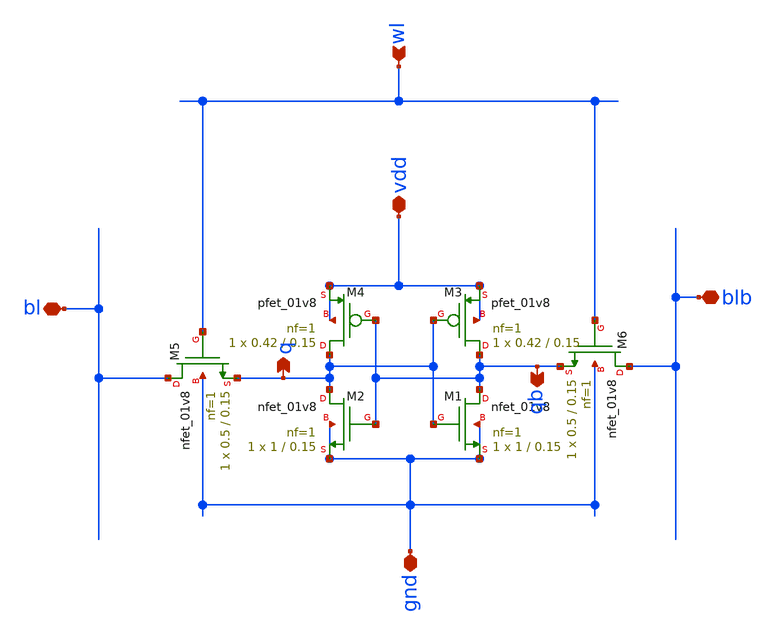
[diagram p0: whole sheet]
** sch_path: schem/sram.sch
**.subckt sram blb bl vdd gnd wl q qb
*.iopin blb
*.iopin bl
*.iopin vdd
*.iopin gnd
*.ipin wl
*.opin q
*.opin qb
XM1 qb q gnd gnd sky130_fd_pr__nfet_01v8 L=0.15 W=1 nf=1 ad='int((nf+1)/2) * W/nf * 0.29' as='int((nf+2)/2) * W/nf * 0.29'
+ pd='2*int((nf+1)/2) * (W/nf + 0.29)' ps='2*int((nf+2)/2) * (W/nf + 0.29)' nrd='0.29 / W' nrs='0.29 / W'
+ sa=0 sb=0 sd=0 mult=1 m=1
XM3 qb q vdd vdd sky130_fd_pr__pfet_01v8 L=0.15 W=0.42 nf=1 ad='int((nf+1)/2) * W/nf * 0.29' as='int((nf+2)/2) * W/nf * 0.29'
+ pd='2*int((nf+1)/2) * (W/nf + 0.29)' ps='2*int((nf+2)/2) * (W/nf + 0.29)' nrd='0.29 / W' nrs='0.29 / W'
+ sa=0 sb=0 sd=0 mult=1 m=1
XM4 q qb vdd vdd sky130_fd_pr__pfet_01v8 L=0.15 W=0.42 nf=1 ad='int((nf+1)/2) * W/nf * 0.29' as='int((nf+2)/2) * W/nf * 0.29'
+ pd='2*int((nf+1)/2) * (W/nf + 0.29)' ps='2*int((nf+2)/2) * (W/nf + 0.29)' nrd='0.29 / W' nrs='0.29 / W'
+ sa=0 sb=0 sd=0 mult=1 m=1
XM2 q qb gnd gnd sky130_fd_pr__nfet_01v8 L=0.15 W=1 nf=1 ad='int((nf+1)/2) * W/nf * 0.29' as='int((nf+2)/2) * W/nf * 0.29'
+ pd='2*int((nf+1)/2) * (W/nf + 0.29)' ps='2*int((nf+2)/2) * (W/nf + 0.29)' nrd='0.29 / W' nrs='0.29 / W'
+ sa=0 sb=0 sd=0 mult=1 m=1
XM5 bl wl q gnd sky130_fd_pr__nfet_01v8 L=0.15 W=0.5 nf=1 ad='int((nf+1)/2) * W/nf * 0.29' as='int((nf+2)/2) * W/nf * 0.29'
+ pd='2*int((nf+1)/2) * (W/nf + 0.29)' ps='2*int((nf+2)/2) * (W/nf + 0.29)' nrd='0.29 / W' nrs='0.29 / W'
+ sa=0 sb=0 sd=0 mult=1 m=1
XM6 blb wl qb gnd sky130_fd_pr__nfet_01v8 L=0.15 W=0.5 nf=1 ad='int((nf+1)/2) * W/nf * 0.29' as='int((nf+2)/2) * W/nf * 0.29'
+ pd='2*int((nf+1)/2) * (W/nf + 0.29)' ps='2*int((nf+2)/2) * (W/nf + 0.29)' nrd='0.29 / W' nrs='0.29 / W'
+ sa=0 sb=0 sd=0 mult=1 m=1
**.ends
.end
